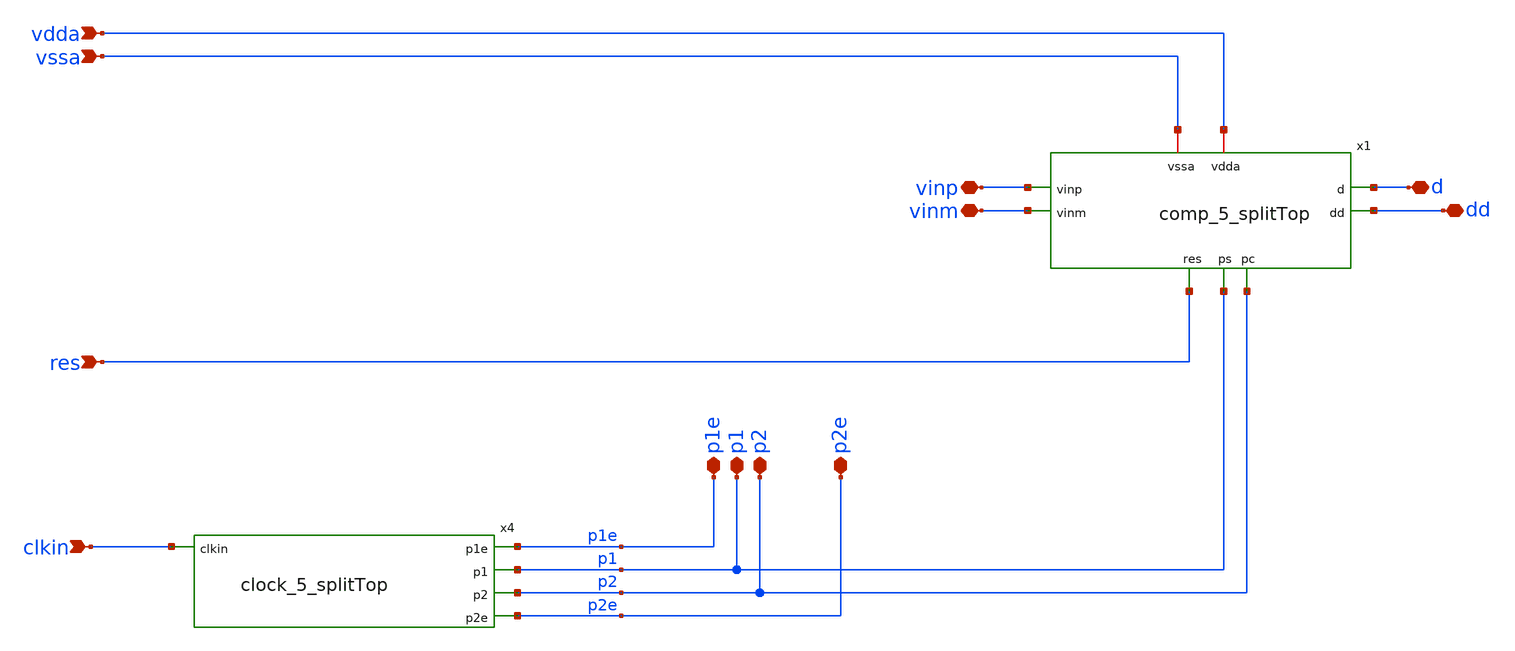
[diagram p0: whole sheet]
** sch_path: 5_Design/4_Layout/Team 5/xschem/Team5_split2.sch
**.subckt Team5_split2 vdda vssa res clkin vinp vinm p1e p1 p2 p2e d dd
*.ipin vdda
*.ipin vssa
*.ipin res
*.ipin clkin
*.iopin vinp
*.iopin vinm
*.iopin p1e
*.iopin p1
*.iopin p2
*.iopin p2e
*.iopin d
*.iopin dd
x1 vdda p2 d dd vinp vssa res p1 vinm comp_5_splitTop
x4 p1e clkin p1 p2 p2e clock_5_splitTop
**.ends
.end
